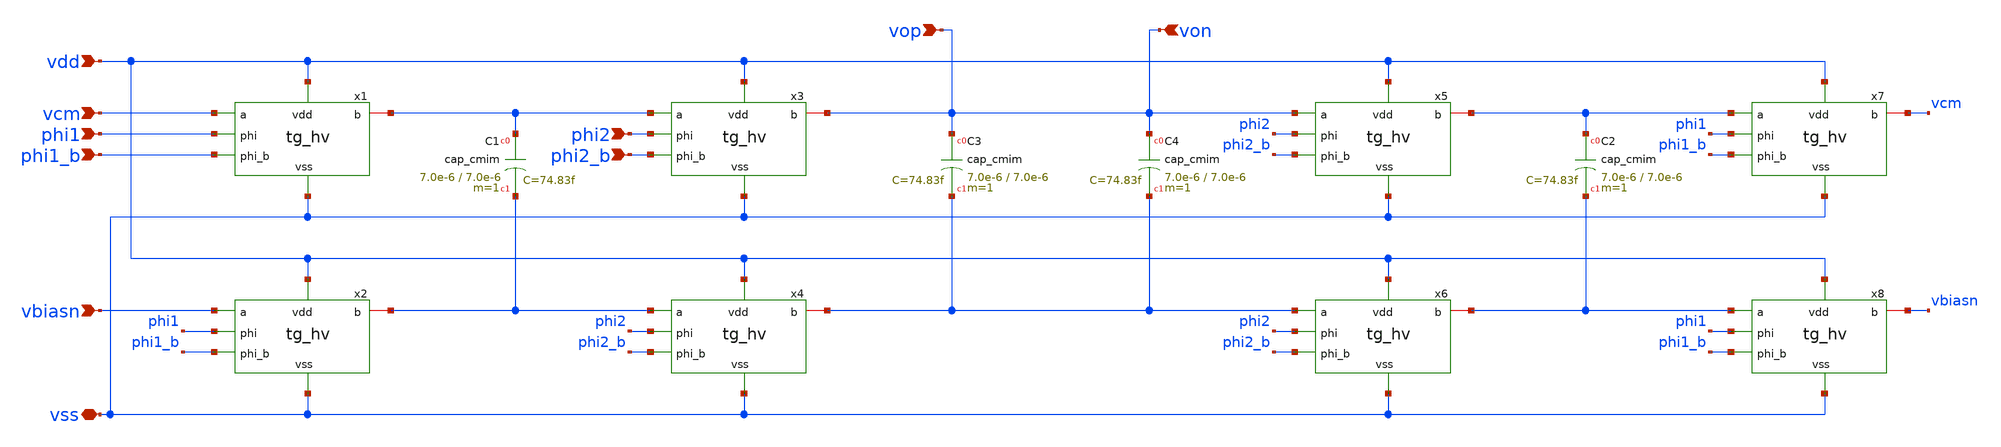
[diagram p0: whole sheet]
** sch_path: 3_real_circuits/sc_cmfb.sch
**.subckt sc_cmfb vcm vbiasn vop von vdd vss phi1 phi1_b phi2_b phi2
*.ipin vcm
*.ipin vbiasn
*.ipin vop
*.ipin von
*.ipin vdd
*.iopin vss
*.ipin phi1
*.ipin phi1_b
*.ipin phi2_b
*.ipin phi2
x1 vcm phi1 phi1_b vop vop vss tg_hv
XC1 vop vop cap_cmim w=7.0e-6 l=7.0e-6 m=1 mm_ok=1
x2 vbiasn phi1 phi1_b vop vop vss tg_hv
x3 vop phi2 phi2_b vop vop vss tg_hv
XC3 vop vop cap_cmim w=7.0e-6 l=7.0e-6 m=1 mm_ok=1
x4 vop phi2 phi2_b vop vop vss tg_hv
XC4 vop vop cap_cmim w=7.0e-6 l=7.0e-6 m=1 mm_ok=1
x5 vop phi2 phi2_b vop vop vss tg_hv
x6 vop phi2 phi2_b vop vop vss tg_hv
XC2 vop vop cap_cmim w=7.0e-6 l=7.0e-6 m=1 mm_ok=1
x7 vop phi1 phi1_b vop vop vss tg_hv
x8 vop phi1 phi1_b vop vop vss tg_hv
**.ends

* expanding   symbol:  tg_hv.sym # of pins=7
** sym_path: 3_real_circuits/tg_hv.sym
** sch_path: 3_real_circuits/tg_hv.sch
.subckt tg_hv a phi phi_b vdd b vss
*.ipin phi_b
*.ipin phi
*.ipin a
*.ipin b
*.ipin vdd
*.iopin vss
XM2 a phi_b b vdd sg13_hv_pmos w=10u l=0.45u ng=1 m=1 mm_ok=1
XM1 a phi b vss sg13_hv_nmos w=5u l=0.45u ng=1 m=1 mm_ok=1
.ends

.end
